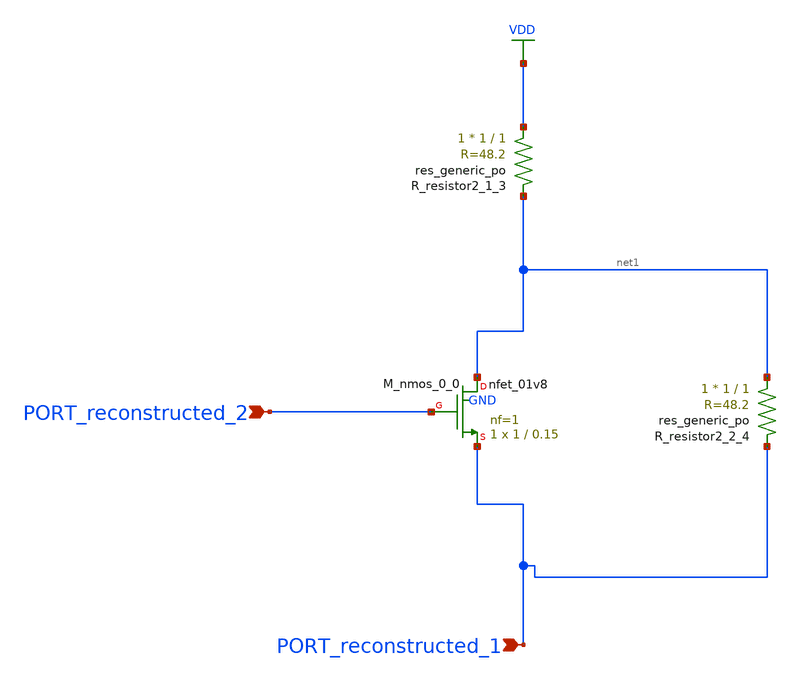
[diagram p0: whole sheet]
** sch_path: schematics/AMSNet/591.sch
**.subckt 591 PORT_reconstructed_2 PORT_reconstructed_1
*.ipin PORT_reconstructed_2
*.ipin PORT_reconstructed_1
XM_nmos_0_0 net1 PORT_reconstructed_2 PORT_reconstructed_1 GND sky130_fd_pr__nfet_01v8 L=0.15 W=1 nf=1
+ ad='int((1 + 1)/2) * 1 / 1 * 0.29' as='int((1 + 2)/2) * 1 / 1 * 0.29' pd='2*int((1 + 1)/2) * (1 / 1 + 0.29)'
+ ps='2*int((1 + 2)/2) * (1 / 1 + 0.29)' nrd='0.29 / 1 ' nrs='0.29 / 1 ' sa=0 sb=0 sd=0 mult=1 m=1
XR_resistor2_1_3 VDD net1 sky130_fd_pr__res_generic_po W=1 L=1 m=1
XR_resistor2_2_4 net1 PORT_reconstructed_1 sky130_fd_pr__res_generic_po W=1 L=1 m=1
**.ends
.GLOBAL VDD
.end
